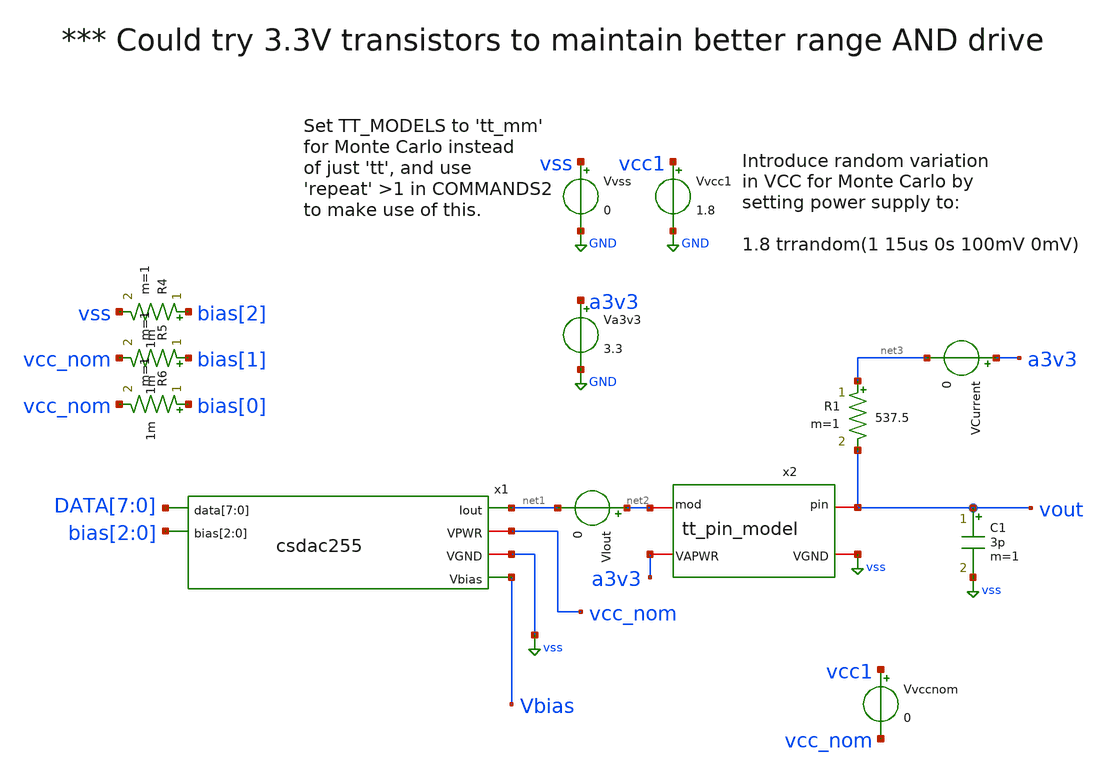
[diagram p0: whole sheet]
** sch_path: xschem/tb_csdac255.sch
**.subckt tb_csdac255
x1 DATA[7] DATA[6] DATA[5] DATA[4] DATA[3] DATA[2] DATA[1] DATA[0] net1 vcc_nom vss Vbias bias[2]
+ bias[1] bias[0] csdac255
Vvcc1 vcc1 GND 1.8
Vvss vss GND 0
Vvccnom vcc1 vcc_nom 0
C1 vout vss 3p m=1
VCurrent a3v3 net3 0
R1 net3 vout 537.5 m=1
VIout net2 net1 0
R4 bias[2] vss 1m m=1
R5 bias[1] vcc_nom 1m m=1
R6 bias[0] vcc_nom 1m m=1
Va3v3 a3v3 GND 3.3
x2 vss a3v3 vout net2 tt_pin_model
**** begin user architecture code



.param singlebits=0
.IF (singlebits == 1)
* Mode to just test each binary-weighted level:
Vxp0 DATA[0]  GND pulse 0v 1.8v 1u 1n 1n 1u 10u
Vxp1 DATA[1]  GND pulse 0v 1.8v 2u 1n 1n 1u 10u
Vxp2 DATA[2]  GND pulse 0v 1.8v 3u 1n 1n 1u 10u
Vxp3 DATA[3]  GND pulse 0v 1.8v 4u 1n 1n 1u 10u
Vxp4 DATA[4]  GND pulse 0v 1.8v 5u 1n 1n 1u 10u
Vxp5 DATA[5]  GND pulse 0v 1.8v 6u 1n 1n 1u 10u
Vxp6 DATA[6]  GND pulse 0v 1.8v 7u 1n 1n 1u 10u
Vxp7 DATA[7]  GND pulse 0v 1.8v 8u 1n 1n 1u 10u
Vxn0 DATAn[0] GND pulse 1.8v 0v 1u 1n 1n 1u 10u
Vxn1 DATAn[1] GND pulse 1.8v 0v 2u 1n 1n 1u 10u
Vxn2 DATAn[2] GND pulse 1.8v 0v 3u 1n 1n 1u 10u
Vxn3 DATAn[3] GND pulse 1.8v 0v 4u 1n 1n 1u 10u
Vxn4 DATAn[4] GND pulse 1.8v 0v 5u 1n 1n 1u 10u
Vxn5 DATAn[5] GND pulse 1.8v 0v 6u 1n 1n 1u 10u
Vxn6 DATAn[6] GND pulse 1.8v 0v 7u 1n 1n 1u 10u
Vxn7 DATAn[7] GND pulse 1.8v 0v 8u 1n 1n 1u 10u
.ELSEIF (singlebits == 0)
* Mode to test full 0..255 trange:
Vxp0 DATA[0]  GND pulse 1.8v 0v 0n 1n 1n 39n 80n
Vxp1 DATA[1]  GND pulse 1.8v 0v 0n 1n 1n 79n 160n
Vxp2 DATA[2]  GND pulse 1.8v 0v 0n 1n 1n 159n 320n
Vxp3 DATA[3]  GND pulse 1.8v 0v 0n 1n 1n 319n 640n
Vxp4 DATA[4]  GND pulse 1.8v 0v 0n 1n 1n 639n 1280n
Vxp5 DATA[5]  GND pulse 1.8v 0v 0n 1n 1n 1279n 2560n
Vxp6 DATA[6]  GND pulse 1.8v 0v 0n 1n 1n 2559n 5120n
Vxp7 DATA[7]  GND pulse 1.8v 0v 0n 1n 1n 5119n 10240n
Vxn0 DATAn[0] GND pulse 0v 1.8v 0n 1n 1n 39n 80n
Vxn1 DATAn[1] GND pulse 0v 1.8v 0n 1n 1n 79n 160n
Vxn2 DATAn[2] GND pulse 0v 1.8v 0n 1n 1n 159n 320n
Vxn3 DATAn[3] GND pulse 0v 1.8v 0n 1n 1n 319n 640n
Vxn4 DATAn[4] GND pulse 0v 1.8v 0n 1n 1n 639n 1280n
Vxn5 DATAn[5] GND pulse 0v 1.8v 0n 1n 1n 1279n 2560n
Vxn6 DATAn[6] GND pulse 0v 1.8v 0n 1n 1n 2559n 5120n
Vxn7 DATAn[7] GND pulse 0v 1.8v 0n 1n 1n 5119n 10240n
.ENDIF

*.options savecurrents
.control
	repeat 10

		save i(vvss) vcc1 vbias vout i(vvccnom) i(vcurrent) i(viout)
		tran 0.1n 12.8u
		*12.8u
		write tb_csdac255.raw i(vvss) vcc1 vbias vout i(vvccnom) i(vcurrent) i(viout)
		* + v(DATA[0]) v(DATA[1]) v(DATA[2]) v(DATA[3]) v(DATA[4]) v(DATA[5]) v(DATA[6]) v(DATA[7])
		set appendwrite
		reset
	end
.endc



 .lib $::SKYWATER_MODELS/sky130.lib.spice tt_mm

.include $::SKYWATER_STDCELLS/sky130_fd_sc_hd.spice

**** end user architecture code
**.ends

* expanding   symbol:  csdac255.sym # of pins=6
** sym_path: xschem/csdac255.sym
** sch_path: xschem/csdac255.sch
.subckt csdac255 data[7] data[6] data[5] data[4] data[3] data[2] data[1] data[0] Iout VPWR VGND
+ Vbias bias[2] bias[1] bias[0]
*.iopin VPWR
*.opin Iout
*.iopin VGND
*.ipin bias[2],bias[1],bias[0]
*.ipin data[7],data[6],data[5],data[4],data[3],data[2],data[1],data[0]
*.opin Vbias
x1 VPWR VGND VPWR VGND THERMO_ROWn[14] THERMO_ROWn[13] THERMO_ROWn[12] THERMO_ROWn[11]
+ THERMO_ROWn[10] THERMO_ROWn[9] THERMO_ROWn[8] THERMO_ROWn[7] THERMO_ROWn[6] THERMO_ROWn[5] THERMO_ROWn[4]
+ THERMO_ROWn[3] THERMO_ROWn[2] THERMO_ROWn[1] THERMO_ROWn[0] data[7] data[6] data[5] data[4] thermo15
x2 VPWR VGND THERMO_ROWn[14] THERMO_ROWn[13] THERMO_ROWn[12] THERMO_ROWn[11] THERMO_ROWn[10]
+ THERMO_ROWn[9] THERMO_ROWn[8] THERMO_ROWn[7] THERMO_ROWn[6] THERMO_ROWn[5] THERMO_ROWn[4] THERMO_ROWn[3]
+ THERMO_ROWn[2] THERMO_ROWn[1] THERMO_ROWn[0] THERMO_COLn[14] THERMO_COLn[13] THERMO_COLn[12] THERMO_COLn[11]
+ THERMO_COLn[10] THERMO_COLn[9] THERMO_COLn[8] THERMO_COLn[7] THERMO_COLn[6] THERMO_COLn[5] THERMO_COLn[4]
+ THERMO_COLn[3] THERMO_COLn[2] THERMO_COLn[1] THERMO_COLn[0] Vbias Iout array255x
x3 VPWR VGND VPWR VGND THERMO_COLn[14] THERMO_COLn[13] THERMO_COLn[12] THERMO_COLn[11]
+ THERMO_COLn[10] THERMO_COLn[9] THERMO_COLn[8] THERMO_COLn[7] THERMO_COLn[6] THERMO_COLn[5] THERMO_COLn[4]
+ THERMO_COLn[3] THERMO_COLn[2] THERMO_COLn[1] THERMO_COLn[0] data[3] data[2] data[1] data[0] thermo15
XMmirror Vbias Vbias VGND VGND sky130_fd_pr__nfet_01v8 L=0.5 W=0.5 nf=1 ad='int((nf+1)/2) * W/nf * 0.29'
+ as='int((nf+2)/2) * W/nf * 0.29' pd='2*int((nf+1)/2) * (W/nf + 0.29)' ps='2*int((nf+2)/2) * (W/nf + 0.29)'
+ nrd='0.29 / W' nrs='0.29 / W' sa=0 sb=0 sd=0 mult=1 m=1
XM1 Vbias bias[2] VPWR VPWR sky130_fd_pr__pfet_01v8 L=0.5 W=0.5 nf=1 ad='int((nf+1)/2) * W/nf * 0.29'
+ as='int((nf+2)/2) * W/nf * 0.29' pd='2*int((nf+1)/2) * (W/nf + 0.29)' ps='2*int((nf+2)/2) * (W/nf + 0.29)'
+ nrd='0.29 / W' nrs='0.29 / W' sa=0 sb=0 sd=0 mult=1 m=1
XM2 Vbias bias[1] VPWR VPWR sky130_fd_pr__pfet_01v8 L=1 W=0.5 nf=1 ad='int((nf+1)/2) * W/nf * 0.29' as='int((nf+2)/2) * W/nf * 0.29'
+ pd='2*int((nf+1)/2) * (W/nf + 0.29)' ps='2*int((nf+2)/2) * (W/nf + 0.29)' nrd='0.29 / W' nrs='0.29 / W'
+ sa=0 sb=0 sd=0 mult=1 m=1
XM3 Vbias bias[0] VPWR VPWR sky130_fd_pr__pfet_01v8 L=2 W=0.5 nf=1 ad='int((nf+1)/2) * W/nf * 0.29' as='int((nf+2)/2) * W/nf * 0.29'
+ pd='2*int((nf+1)/2) * (W/nf + 0.29)' ps='2*int((nf+2)/2) * (W/nf + 0.29)' nrd='0.29 / W' nrs='0.29 / W'
+ sa=0 sb=0 sd=0 mult=1 m=1
.ends


* expanding   symbol:  tt_pin_model.sym # of pins=4
** sym_path: xschem/tt_pin_model.sym
** sch_path: xschem/tt_pin_model.sch
.subckt tt_pin_model VGND VAPWR pin mod
*.iopin VGND
*.iopin VAPWR
*.iopin mod
*.iopin pin
R2 net1 pin 1 m=1
C2 pin VGND 1p m=1
L7 net2 net1 1n m=1
C3 net2 VGND 2p m=1
R3 net3 net2 50 m=1
C4 net3 VGND 250f m=1
XM2 net3 VGND mod VAPWR sky130_fd_pr__pfet_g5v0d10v5 L=0.5 W=100 nf=20 ad='int((nf+1)/2) * W/nf * 0.29'
+ as='int((nf+2)/2) * W/nf * 0.29' pd='2*int((nf+1)/2) * (W/nf + 0.29)' ps='2*int((nf+2)/2) * (W/nf + 0.29)'
+ nrd='0.29 / W' nrs='0.29 / W' sa=0 sb=0 sd=0 mult=1 m=1
XM1 net3 VAPWR mod VGND sky130_fd_pr__nfet_g5v0d10v5 L=0.5 W=60 nf=12 ad='int((nf+1)/2) * W/nf * 0.29'
+ as='int((nf+2)/2) * W/nf * 0.29' pd='2*int((nf+1)/2) * (W/nf + 0.29)' ps='2*int((nf+2)/2) * (W/nf + 0.29)'
+ nrd='0.29 / W' nrs='0.29 / W' sa=0 sb=0 sd=0 mult=1 m=1
XM4 net3 VAPWR VGND VAPWR sky130_fd_pr__pfet_g5v0d10v5 L=0.5 W=100 nf=20 ad='int((nf+1)/2) * W/nf * 0.29'
+ as='int((nf+2)/2) * W/nf * 0.29' pd='2*int((nf+1)/2) * (W/nf + 0.29)' ps='2*int((nf+2)/2) * (W/nf + 0.29)'
+ nrd='0.29 / W' nrs='0.29 / W' sa=0 sb=0 sd=0 mult=15 m=15
XM3 net3 VGND VGND VGND sky130_fd_pr__nfet_g5v0d10v5 L=0.5 W=60 nf=12 ad='int((nf+1)/2) * W/nf * 0.29'
+ as='int((nf+2)/2) * W/nf * 0.29' pd='2*int((nf+1)/2) * (W/nf + 0.29)' ps='2*int((nf+2)/2) * (W/nf + 0.29)'
+ nrd='0.29 / W' nrs='0.29 / W' sa=0 sb=0 sd=0 mult=15 m=15
C5 mod VGND 250f m=1
.ends


* expanding   symbol:  thermo15.sym # of pins=6
** sym_path: xschem/thermo15.sym
** sch_path: xschem/thermo15.sch
.subckt thermo15 VPWR VGND VPB VNB Tn[14] Tn[13] Tn[12] Tn[11] Tn[10] Tn[9] Tn[8] Tn[7] Tn[6] Tn[5]
+ Tn[4] Tn[3] Tn[2] Tn[1] Tn[0] d[3] d[2] d[1] d[0]
*.iopin VPWR
*.ipin d[3],d[2],d[1],d[0]
*.iopin VGND
*.iopin VPB
*.iopin VNB
*.opin
*+ Tn[14],Tn[13],Tn[12],Tn[11],Tn[10],Tn[9],Tn[8],Tn[7],Tn[6],Tn[5],Tn[4],Tn[3],Tn[2],Tn[1],Tn[0]
x1 d[1] VGND VNB VPB VPWR net3 sky130_fd_sc_hd__inv_1
x2 net5 VGND VNB VPB VPWR net6 sky130_fd_sc_hd__inv_2
x3 d[0] d[1] VGND VNB VPB VPWR net4 sky130_fd_sc_hd__nand2_1
x4 d[0] d[1] VGND VNB VPB VPWR net2 sky130_fd_sc_hd__nor2_1
x5 d[2] VGND VNB VPB VPWR net1 sky130_fd_sc_hd__inv_1
x6 net2 net1 VGND VNB VPB VPWR net7 sky130_fd_sc_hd__nand2_1
x7 net3 net1 VGND VNB VPB VPWR net8 sky130_fd_sc_hd__nand2_1
x8 net4 net1 VGND VNB VPB VPWR net9 sky130_fd_sc_hd__nand2_1
x9 net1 VGND VNB VPB VPWR net10 sky130_fd_sc_hd__inv_1
x10 net2 net1 VGND VNB VPB VPWR net11 sky130_fd_sc_hd__nor2_1
x11 net3 net1 VGND VNB VPB VPWR net12 sky130_fd_sc_hd__nor2_1
x12 net4 net1 VGND VNB VPB VPWR net13 sky130_fd_sc_hd__nor2_1
x13 net7 net6 VGND VNB VPB VPWR Tn[0] sky130_fd_sc_hd__nor2_4
x14 net8 net6 VGND VNB VPB VPWR Tn[1] sky130_fd_sc_hd__nor2_4
x15 net9 net6 VGND VNB VPB VPWR Tn[2] sky130_fd_sc_hd__nor2_4
x16 net10 net6 VGND VNB VPB VPWR Tn[3] sky130_fd_sc_hd__nor2_4
x17 net11 net6 VGND VNB VPB VPWR Tn[4] sky130_fd_sc_hd__nor2_4
x18 net12 net6 VGND VNB VPB VPWR Tn[5] sky130_fd_sc_hd__nor2_4
x19 net13 net6 VGND VNB VPB VPWR Tn[6] sky130_fd_sc_hd__nor2_4
x20 net6 VGND VNB VPB VPWR Tn[7] sky130_fd_sc_hd__inv_4
x21 net7 net6 VGND VNB VPB VPWR Tn[8] sky130_fd_sc_hd__nand2_4
x22 net8 net6 VGND VNB VPB VPWR Tn[9] sky130_fd_sc_hd__nand2_4
x23 net9 net6 VGND VNB VPB VPWR Tn[10] sky130_fd_sc_hd__nand2_4
x24 net10 net6 VGND VNB VPB VPWR Tn[11] sky130_fd_sc_hd__nand2_4
x25 net11 net6 VGND VNB VPB VPWR Tn[12] sky130_fd_sc_hd__nand2_4
x26 net12 net6 VGND VNB VPB VPWR Tn[13] sky130_fd_sc_hd__nand2_4
x27 net13 net6 VGND VNB VPB VPWR Tn[14] sky130_fd_sc_hd__nand2_4
x28 d[3] VGND VNB VPB VPWR net5 sky130_fd_sc_hd__inv_1
.ends


* expanding   symbol:  array255x.sym # of pins=6
** sym_path: xschem/array255x.sym
** sch_path: xschem/array255x.sch
.subckt array255x VPWR VGND Rn[14] Rn[13] Rn[12] Rn[11] Rn[10] Rn[9] Rn[8] Rn[7] Rn[6] Rn[5] Rn[4]
+ Rn[3] Rn[2] Rn[1] Rn[0] Cn[14] Cn[13] Cn[12] Cn[11] Cn[10] Cn[9] Cn[8] Cn[7] Cn[6] Cn[5] Cn[4] Cn[3]
+ Cn[2] Cn[1] Cn[0] Vbias Iout
*.iopin VPWR
*.opin Iout
*.iopin VGND
*.ipin Vbias
*.ipin
*+ Cn[14],Cn[13],Cn[12],Cn[11],Cn[10],Cn[9],Cn[8],Cn[7],Cn[6],Cn[5],Cn[4],Cn[3],Cn[2],Cn[1],Cn[0]
*.ipin
*+ Rn[14],Rn[13],Rn[12],Rn[11],Rn[10],Rn[9],Rn[8],Rn[7],Rn[6],Rn[5],Rn[4],Rn[3],Rn[2],Rn[1],Rn[0]
XIR[14] Vbias VPWR Rn[14] Rn[13] Cn[14] Cn[13] Cn[12] Cn[11] Cn[10] Cn[9] Cn[8] Cn[7] Cn[6] Cn[5]
+ Cn[4] Cn[3] Cn[2] Cn[1] Cn[0] VGND Iout row15x
XIR[13] Vbias VPWR Rn[13] Rn[12] Cn[14] Cn[13] Cn[12] Cn[11] Cn[10] Cn[9] Cn[8] Cn[7] Cn[6] Cn[5]
+ Cn[4] Cn[3] Cn[2] Cn[1] Cn[0] VGND Iout row15x
XIR[12] Vbias VPWR Rn[12] Rn[11] Cn[14] Cn[13] Cn[12] Cn[11] Cn[10] Cn[9] Cn[8] Cn[7] Cn[6] Cn[5]
+ Cn[4] Cn[3] Cn[2] Cn[1] Cn[0] VGND Iout row15x
XIR[11] Vbias VPWR Rn[11] Rn[10] Cn[14] Cn[13] Cn[12] Cn[11] Cn[10] Cn[9] Cn[8] Cn[7] Cn[6] Cn[5]
+ Cn[4] Cn[3] Cn[2] Cn[1] Cn[0] VGND Iout row15x
XIR[10] Vbias VPWR Rn[10] Rn[9] Cn[14] Cn[13] Cn[12] Cn[11] Cn[10] Cn[9] Cn[8] Cn[7] Cn[6] Cn[5]
+ Cn[4] Cn[3] Cn[2] Cn[1] Cn[0] VGND Iout row15x
XIR[9] Vbias VPWR Rn[9] Rn[8] Cn[14] Cn[13] Cn[12] Cn[11] Cn[10] Cn[9] Cn[8] Cn[7] Cn[6] Cn[5] Cn[4]
+ Cn[3] Cn[2] Cn[1] Cn[0] VGND Iout row15x
XIR[8] Vbias VPWR Rn[8] Rn[7] Cn[14] Cn[13] Cn[12] Cn[11] Cn[10] Cn[9] Cn[8] Cn[7] Cn[6] Cn[5] Cn[4]
+ Cn[3] Cn[2] Cn[1] Cn[0] VGND Iout row15x
XIR[7] Vbias VPWR Rn[7] Rn[6] Cn[14] Cn[13] Cn[12] Cn[11] Cn[10] Cn[9] Cn[8] Cn[7] Cn[6] Cn[5] Cn[4]
+ Cn[3] Cn[2] Cn[1] Cn[0] VGND Iout row15x
XIR[6] Vbias VPWR Rn[6] Rn[5] Cn[14] Cn[13] Cn[12] Cn[11] Cn[10] Cn[9] Cn[8] Cn[7] Cn[6] Cn[5] Cn[4]
+ Cn[3] Cn[2] Cn[1] Cn[0] VGND Iout row15x
XIR[5] Vbias VPWR Rn[5] Rn[4] Cn[14] Cn[13] Cn[12] Cn[11] Cn[10] Cn[9] Cn[8] Cn[7] Cn[6] Cn[5] Cn[4]
+ Cn[3] Cn[2] Cn[1] Cn[0] VGND Iout row15x
XIR[4] Vbias VPWR Rn[4] Rn[3] Cn[14] Cn[13] Cn[12] Cn[11] Cn[10] Cn[9] Cn[8] Cn[7] Cn[6] Cn[5] Cn[4]
+ Cn[3] Cn[2] Cn[1] Cn[0] VGND Iout row15x
XIR[3] Vbias VPWR Rn[3] Rn[2] Cn[14] Cn[13] Cn[12] Cn[11] Cn[10] Cn[9] Cn[8] Cn[7] Cn[6] Cn[5] Cn[4]
+ Cn[3] Cn[2] Cn[1] Cn[0] VGND Iout row15x
XIR[2] Vbias VPWR Rn[2] Rn[1] Cn[14] Cn[13] Cn[12] Cn[11] Cn[10] Cn[9] Cn[8] Cn[7] Cn[6] Cn[5] Cn[4]
+ Cn[3] Cn[2] Cn[1] Cn[0] VGND Iout row15x
XIR[1] Vbias VPWR Rn[1] Rn[0] Cn[14] Cn[13] Cn[12] Cn[11] Cn[10] Cn[9] Cn[8] Cn[7] Cn[6] Cn[5] Cn[4]
+ Cn[3] Cn[2] Cn[1] Cn[0] VGND Iout row15x
XIR[0] Vbias VPWR Rn[0] VGND Cn[14] Cn[13] Cn[12] Cn[11] Cn[10] Cn[9] Cn[8] Cn[7] Cn[6] Cn[5] Cn[4]
+ Cn[3] Cn[2] Cn[1] Cn[0] VGND Iout row15x
XIR[15] Vbias VPWR VPWR Rn[14] Cn[14] Cn[13] Cn[12] Cn[11] Cn[10] Cn[9] Cn[8] Cn[7] Cn[6] Cn[5]
+ Cn[4] Cn[3] Cn[2] Cn[1] Cn[0] VGND Iout row15x
.ends


* expanding   symbol:  row15x.sym # of pins=7
** sym_path: xschem/row15x.sym
** sch_path: xschem/row15x.sch
.subckt row15x Vbias VPWR Sn Rn Cn[14] Cn[13] Cn[12] Cn[11] Cn[10] Cn[9] Cn[8] Cn[7] Cn[6] Cn[5]
+ Cn[4] Cn[3] Cn[2] Cn[1] Cn[0] VGND Iout
*.ipin Sn
*.ipin Rn
*.ipin
*+ Cn[14],Cn[13],Cn[12],Cn[11],Cn[10],Cn[9],Cn[8],Cn[7],Cn[6],Cn[5],Cn[4],Cn[3],Cn[2],Cn[1],Cn[0]
*.iopin VPWR
*.iopin VGND
*.opin Iout
*.ipin Vbias
XIC[14] VPWR VGND Rn Cn[14] Sn Vbias Iout icell
XIC[13] VPWR VGND Rn Cn[13] Sn Vbias Iout icell
XIC[12] VPWR VGND Rn Cn[12] Sn Vbias Iout icell
XIC[11] VPWR VGND Rn Cn[11] Sn Vbias Iout icell
XIC[10] VPWR VGND Rn Cn[10] Sn Vbias Iout icell
XIC[9] VPWR VGND Rn Cn[9] Sn Vbias Iout icell
XIC[8] VPWR VGND Rn Cn[8] Sn Vbias Iout icell
XIC[7] VPWR VGND Rn Cn[7] Sn Vbias Iout icell
XIC[6] VPWR VGND Rn Cn[6] Sn Vbias Iout icell
XIC[5] VPWR VGND Rn Cn[5] Sn Vbias Iout icell
XIC[4] VPWR VGND Rn Cn[4] Sn Vbias Iout icell
XIC[3] VPWR VGND Rn Cn[3] Sn Vbias Iout icell
XIC[2] VPWR VGND Rn Cn[2] Sn Vbias Iout icell
XIC[1] VPWR VGND Rn Cn[1] Sn Vbias Iout icell
XIC[0] VPWR VGND Rn Cn[0] Sn Vbias Iout icell
XIC[15] VPWR VGND VPWR VPWR Sn Vbias Iout icell
.ends


* expanding   symbol:  icell.sym # of pins=7
** sym_path: xschem/icell.sym
** sch_path: xschem/icell.sch
.subckt icell VPWR VGND Rn Cn Sn Vbias Iout
*.ipin Rn
*.iopin VPWR
*.opin Iout
*.iopin VGND
*.ipin Cn
*.ipin Sn
*.ipin Vbias
XM2 Ien Sn VPWR VPWR sky130_fd_pr__pfet_01v8 L=0.15 W=0.5 nf=1 ad='int((nf+1)/2) * W/nf * 0.29' as='int((nf+2)/2) * W/nf * 0.29'
+ pd='2*int((nf+1)/2) * (W/nf + 0.29)' ps='2*int((nf+2)/2) * (W/nf + 0.29)' nrd='0.29 / W' nrs='0.29 / W'
+ sa=0 sb=0 sd=0 mult=1 m=1
XM3 Ien Sn PDM VGND sky130_fd_pr__nfet_01v8 L=0.15 W=0.5 nf=1 ad='int((nf+1)/2) * W/nf * 0.29' as='int((nf+2)/2) * W/nf * 0.29'
+ pd='2*int((nf+1)/2) * (W/nf + 0.29)' ps='2*int((nf+2)/2) * (W/nf + 0.29)' nrd='0.29 / W' nrs='0.29 / W'
+ sa=0 sb=0 sd=0 mult=1 m=1
XM4 Ien Cn PUM VPWR sky130_fd_pr__pfet_01v8 L=0.15 W=0.5 nf=1 ad='int((nf+1)/2) * W/nf * 0.29' as='int((nf+2)/2) * W/nf * 0.29'
+ pd='2*int((nf+1)/2) * (W/nf + 0.29)' ps='2*int((nf+2)/2) * (W/nf + 0.29)' nrd='0.29 / W' nrs='0.29 / W'
+ sa=0 sb=0 sd=0 mult=1 m=1
XM5 PUM Rn VPWR VPWR sky130_fd_pr__pfet_01v8 L=0.15 W=0.5 nf=1 ad='int((nf+1)/2) * W/nf * 0.29' as='int((nf+2)/2) * W/nf * 0.29'
+ pd='2*int((nf+1)/2) * (W/nf + 0.29)' ps='2*int((nf+2)/2) * (W/nf + 0.29)' nrd='0.29 / W' nrs='0.29 / W'
+ sa=0 sb=0 sd=0 mult=1 m=1
XM6 PDM Rn VGND VGND sky130_fd_pr__nfet_01v8 L=0.15 W=0.5 nf=1 ad='int((nf+1)/2) * W/nf * 0.29' as='int((nf+2)/2) * W/nf * 0.29'
+ pd='2*int((nf+1)/2) * (W/nf + 0.29)' ps='2*int((nf+2)/2) * (W/nf + 0.29)' nrd='0.29 / W' nrs='0.29 / W'
+ sa=0 sb=0 sd=0 mult=1 m=1
XM7 PDM Cn VGND VGND sky130_fd_pr__nfet_01v8 L=0.15 W=0.5 nf=1 ad='int((nf+1)/2) * W/nf * 0.29' as='int((nf+2)/2) * W/nf * 0.29'
+ pd='2*int((nf+1)/2) * (W/nf + 0.29)' ps='2*int((nf+2)/2) * (W/nf + 0.29)' nrd='0.29 / W' nrs='0.29 / W'
+ sa=0 sb=0 sd=0 mult=1 m=1
XM1 SM Vbias VGND VGND sky130_fd_pr__nfet_g5v0d10v5 L=0.5 W=0.5 nf=1 ad='int((nf+1)/2) * W/nf * 0.29'
+ as='int((nf+2)/2) * W/nf * 0.29' pd='2*int((nf+1)/2) * (W/nf + 0.29)' ps='2*int((nf+2)/2) * (W/nf + 0.29)'
+ nrd='0.29 / W' nrs='0.29 / W' sa=0 sb=0 sd=0 mult=1 m=1
XM8 Iout Ien SM VGND sky130_fd_pr__nfet_g5v0d10v5 L=0.5 W=1.0 nf=1 ad='int((nf+1)/2) * W/nf * 0.29' as='int((nf+2)/2) * W/nf * 0.29'
+ pd='2*int((nf+1)/2) * (W/nf + 0.29)' ps='2*int((nf+2)/2) * (W/nf + 0.29)' nrd='0.29 / W' nrs='0.29 / W'
+ sa=0 sb=0 sd=0 mult=1 m=1
.ends

.GLOBAL GND
.GLOBAL vss
.end
